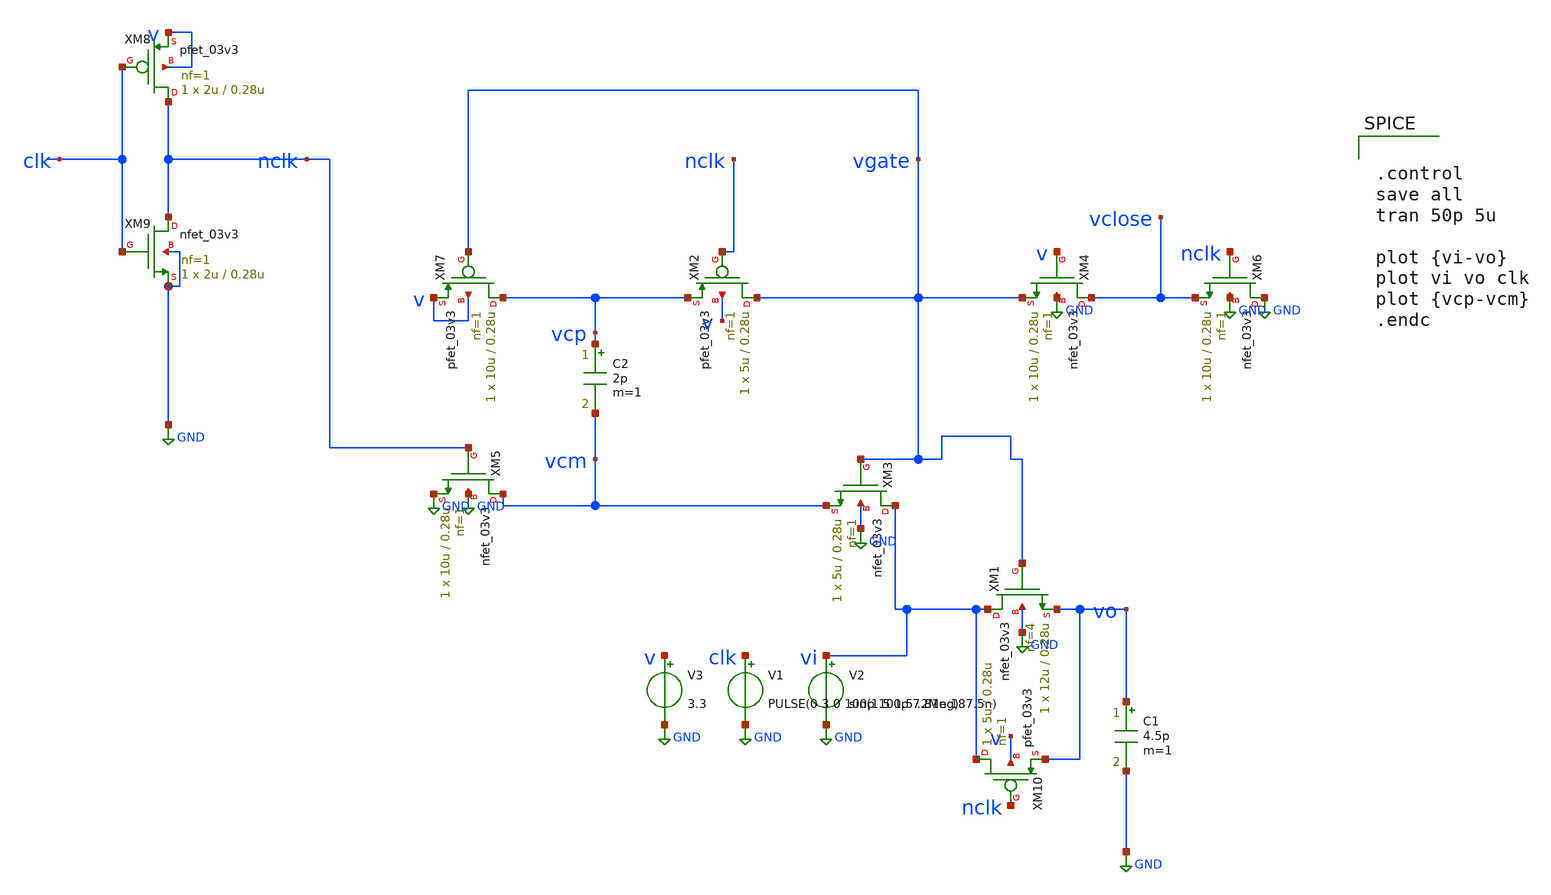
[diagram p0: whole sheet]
** sch_path: SAR_ADC/xschem/test/bootstrap_tb/btsw2_pmos_tb.sch
**.subckt btsw2_pmos_tb
XM1 vi vgate vo GND nfet_03v3 L=0.28u W=12u nf=4 ad='int((nf+1)/2) * W/nf * 0.18u' as='int((nf+2)/2) * W/nf * 0.18u'
+ pd='2*int((nf+1)/2) * (W/nf + 0.18u)' ps='2*int((nf+2)/2) * (W/nf + 0.18u)' nrd='0.18u / W' nrs='0.18u / W'
+ sa=0 sb=0 sd=0 m=1
XM2 vgate nclk vcp v pfet_03v3 L=0.28u W=5u nf=1 ad='int((nf+1)/2) * W/nf * 0.18u' as='int((nf+2)/2) * W/nf * 0.18u'
+ pd='2*int((nf+1)/2) * (W/nf + 0.18u)' ps='2*int((nf+2)/2) * (W/nf + 0.18u)' nrd='0.18u / W' nrs='0.18u / W'
+ sa=0 sb=0 sd=0 m=1
XM3 vi vgate vcm GND nfet_03v3 L=0.28u W=5u nf=1 ad='int((nf+1)/2) * W/nf * 0.18u' as='int((nf+2)/2) * W/nf * 0.18u'
+ pd='2*int((nf+1)/2) * (W/nf + 0.18u)' ps='2*int((nf+2)/2) * (W/nf + 0.18u)' nrd='0.18u / W' nrs='0.18u / W'
+ sa=0 sb=0 sd=0 m=1
XM4 vclose v vgate GND nfet_03v3 L=0.28u W=10u nf=1 ad='int((nf+1)/2) * W/nf * 0.18u' as='int((nf+2)/2) * W/nf * 0.18u'
+ pd='2*int((nf+1)/2) * (W/nf + 0.18u)' ps='2*int((nf+2)/2) * (W/nf + 0.18u)' nrd='0.18u / W' nrs='0.18u / W'
+ sa=0 sb=0 sd=0 m=1
XM5 vcm nclk GND GND nfet_03v3 L=0.28u W=10u nf=1 ad='int((nf+1)/2) * W/nf * 0.18u' as='int((nf+2)/2) * W/nf * 0.18u'
+ pd='2*int((nf+1)/2) * (W/nf + 0.18u)' ps='2*int((nf+2)/2) * (W/nf + 0.18u)' nrd='0.18u / W' nrs='0.18u / W'
+ sa=0 sb=0 sd=0 m=1
XM6 GND nclk vclose GND nfet_03v3 L=0.28u W=10u nf=1 ad='int((nf+1)/2) * W/nf * 0.18u' as='int((nf+2)/2) * W/nf * 0.18u'
+ pd='2*int((nf+1)/2) * (W/nf + 0.18u)' ps='2*int((nf+2)/2) * (W/nf + 0.18u)' nrd='0.18u / W' nrs='0.18u / W'
+ sa=0 sb=0 sd=0 m=1
XM7 vcp vgate v v pfet_03v3 L=0.28u W=10u nf=1 ad='int((nf+1)/2) * W/nf * 0.18u' as='int((nf+2)/2) * W/nf * 0.18u'
+ pd='2*int((nf+1)/2) * (W/nf + 0.18u)' ps='2*int((nf+2)/2) * (W/nf + 0.18u)' nrd='0.18u / W' nrs='0.18u / W'
+ sa=0 sb=0 sd=0 m=1
V1 clk GND PULSE(0 3 0 100p 100p 7.81n 187.5n)
V2 vi GND sin(1.5 1.5 .2Meg)
V3 v GND 3.3
XM8 nclk clk v v pfet_03v3 L=0.28u W=2u nf=1 ad='int((nf+1)/2) * W/nf * 0.18u' as='int((nf+2)/2) * W/nf * 0.18u'
+ pd='2*int((nf+1)/2) * (W/nf + 0.18u)' ps='2*int((nf+2)/2) * (W/nf + 0.18u)' nrd='0.18u / W' nrs='0.18u / W'
+ sa=0 sb=0 sd=0 m=1
XM9 nclk clk GND GND nfet_03v3 L=0.28u W=2u nf=1 ad='int((nf+1)/2) * W/nf * 0.18u' as='int((nf+2)/2) * W/nf * 0.18u'
+ pd='2*int((nf+1)/2) * (W/nf + 0.18u)' ps='2*int((nf+2)/2) * (W/nf + 0.18u)' nrd='0.18u / W' nrs='0.18u / W'
+ sa=0 sb=0 sd=0 m=1
C1 vo GND 4.5p m=1
C2 vcp vcm 2p m=1
XM10 vi nclk vo v pfet_03v3 L=0.28u W=5u nf=1 ad='int((nf+1)/2) * W/nf * 0.18u' as='int((nf+2)/2) * W/nf * 0.18u'
+ pd='2*int((nf+1)/2) * (W/nf + 0.18u)' ps='2*int((nf+2)/2) * (W/nf + 0.18u)' nrd='0.18u / W' nrs='0.18u / W'
+ sa=0 sb=0 sd=0 m=1
**** begin user architecture code


.control
save all
tran 50p 5u

plot {vi-vo}
plot vi vo clk
plot {vcp-vcm}
.endc


.include /foss/pdks/gf180mcuC/libs.tech/ngspice/design.ngspice
.lib /foss/pdks/gf180mcuC/libs.tech/ngspice/sm141064.ngspice typical
.lib /foss/pdks/gf180mcuC/libs.tech/ngspice/sm141064.ngspice mimcap_statistical
.lib /foss/pdks/gf180mcuC/libs.tech/ngspice/sm141064.ngspice cap_mim

**** end user architecture code
**.ends
.GLOBAL GND
.end
